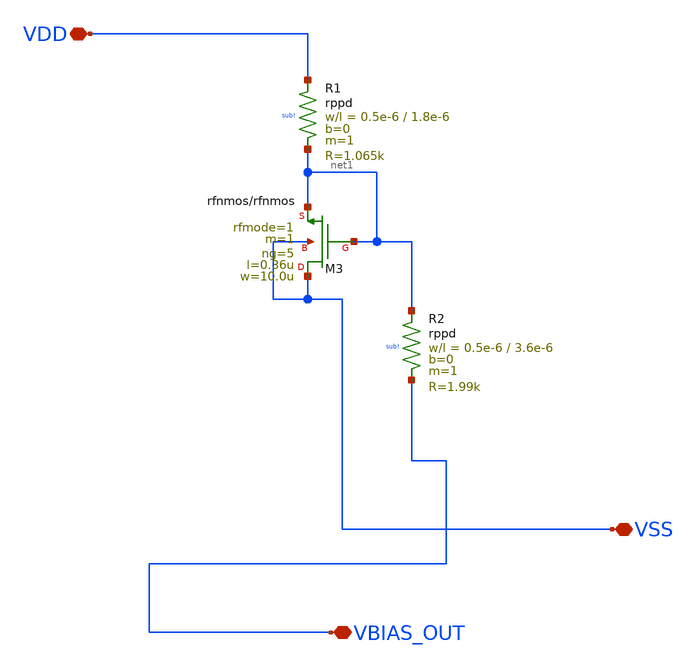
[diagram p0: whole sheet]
** sch_path: GPS_LNA/design_data/lvs/parts/vbias.sch
**.subckt vbias VDD VSS VBIAS_OUT
*.iopin VDD
*.iopin VSS
*.iopin VBIAS_OUT
XR2 net1 VBIAS_OUT sub! rppd w=0.5e-6 l=3.6e-6 m=1 b=0 mm_ok=1
XR1 VDD net1 sub! rppd w=0.5e-6 l=1.8e-6 m=1 b=0 mm_ok=1
XM3 VSS net1 net1 VSS rfnmos w=10.0u l=0.36u ng=5 m=1 rfmode=1 mm_ok=1
**.ends
.end
